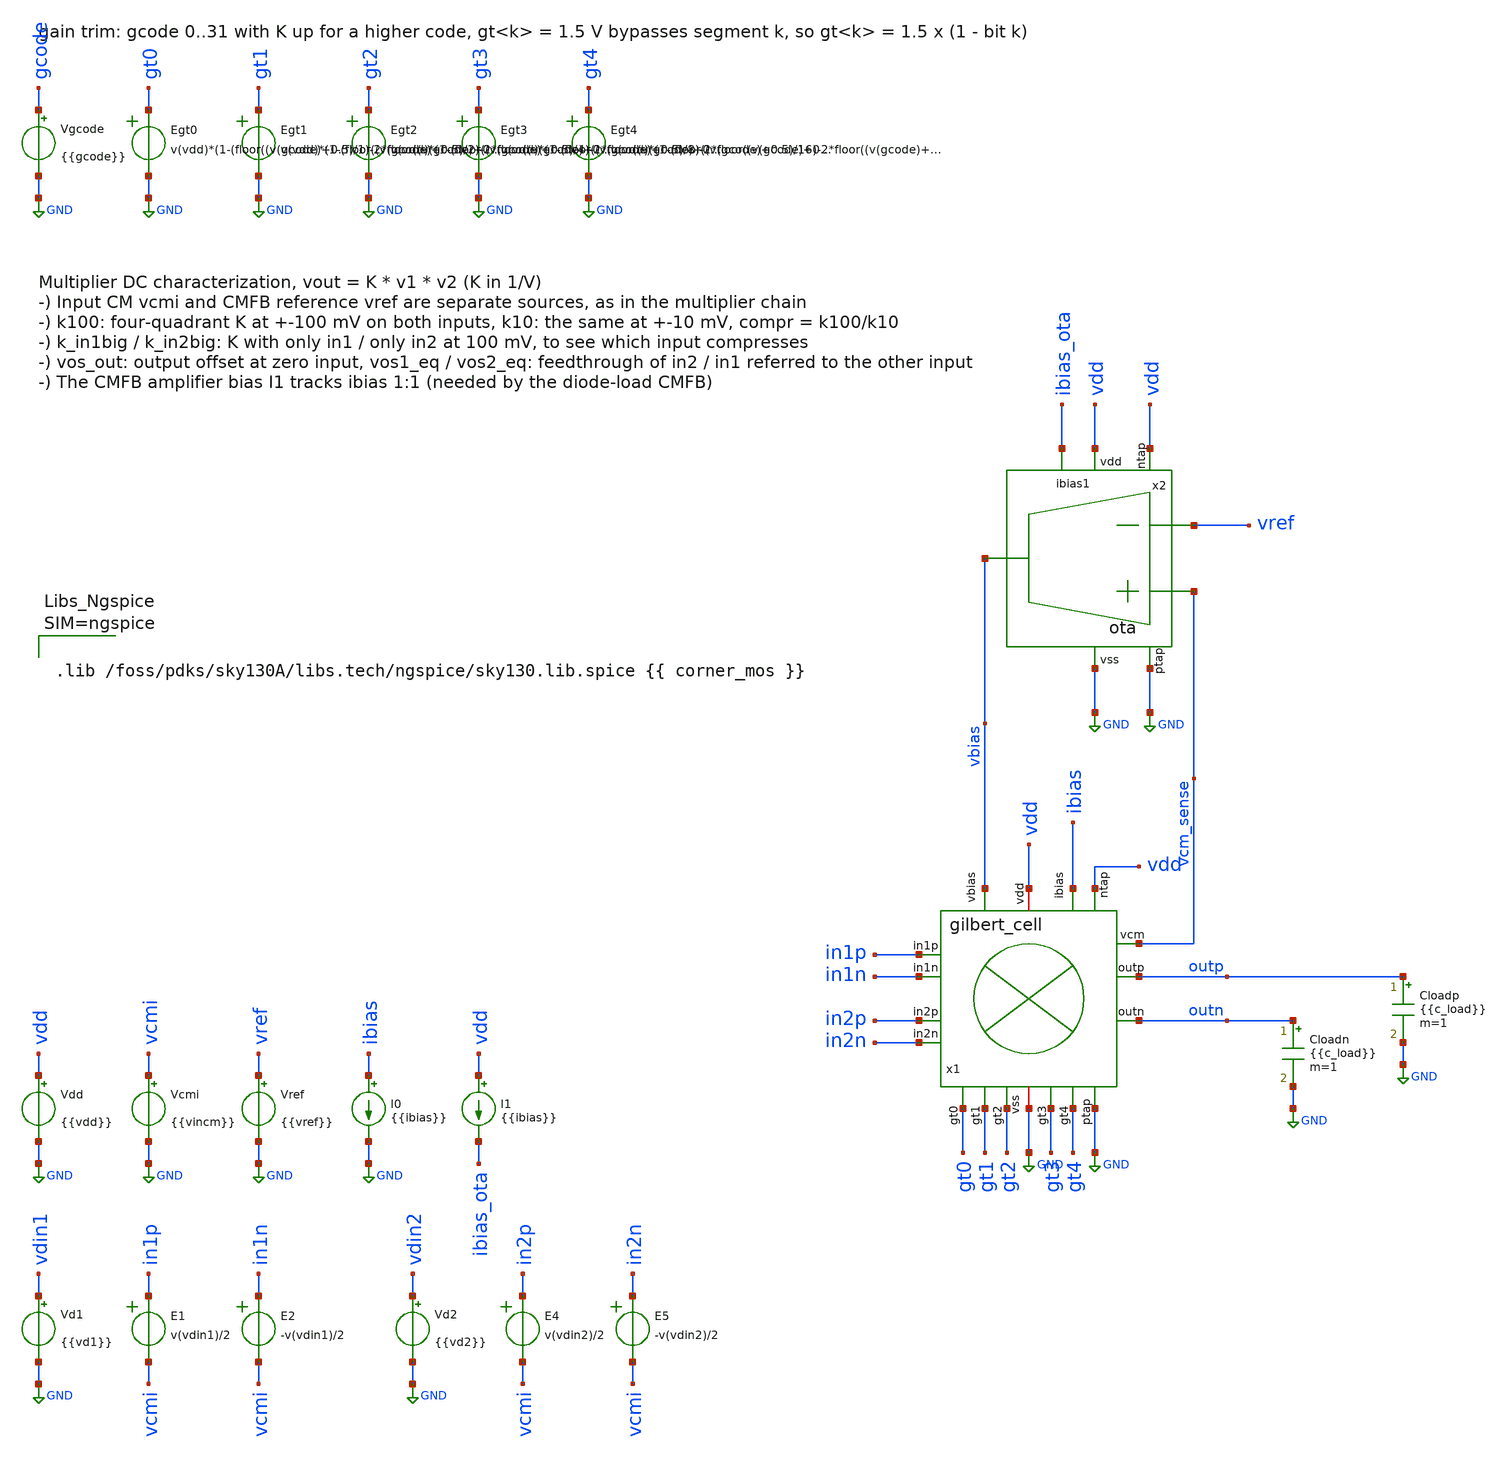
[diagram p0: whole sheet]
** sch_path: verification/porting/sky_gilbert/tb/tb_gilbert_cell_mult.sch
**.subckt tb_gilbert_cell_mult
Vdd vdd GND {{vdd}}
.save i(vdd)
Vcmi vcmi GND {{vincm}}
Vref vref GND {{vref}}
I0 ibias GND {{ibias}}
I1 vdd ibias_ota {{ibias}}
Vd1 vdin1 GND {{vd1}}
E1 in1p vcmi VOL=' v(vdin1)/2 '
E2 in1n vcmi VOL=' -v(vdin1)/2 '
Vd2 vdin2 GND {{vd2}}
E4 in2p vcmi VOL=' v(vdin2)/2 '
E5 in2n vcmi VOL=' -v(vdin2)/2 '
x1 vdd vbias outp outn in1n in1p in2p in2n GND ibias vdd GND vcm_sense gt0 gt1 gt2 gt3 gt4
+ gilbert_cell
Cloadp outp GND {{c_load}} m=1
Cloadn outn GND {{c_load}} m=1
x2 vdd vbias vref vcm_sense GND ibias_ota vdd GND ota
Vgcode gcode GND {{gcode}}
Egt0 gt0 GND VOL=' v(vdd)*(1-(floor((v(gcode)+0.5)/1)-2*floor((v(gcode)+0.5)/2))) '
Egt1 gt1 GND VOL=' v(vdd)*(1-(floor((v(gcode)+0.5)/2)-2*floor((v(gcode)+0.5)/4))) '
Egt2 gt2 GND VOL=' v(vdd)*(1-(floor((v(gcode)+0.5)/4)-2*floor((v(gcode)+0.5)/8))) '
Egt3 gt3 GND VOL=' v(vdd)*(1-(floor((v(gcode)+0.5)/8)-2*floor((v(gcode)+0.5)/16))) '
Egt4 gt4 GND VOL=' v(vdd)*(1-(floor((v(gcode)+0.5)/16)-2*floor((v(gcode)+0.5)/32))) '
**** begin user architecture code


.temp {{ temp }}
.option SEED = {{ (seed|int) + 1 }}
.option method=gear

.control
save all
* op1..op21: (vd1, vd2) points; every op plot gets vout = v(outp)-v(outn)
op
let vout = v(outp)-v(outn)
let vocm = (v(outp)+v(outn))/2
alter vd1 dc=0.1
alter vd2 dc=0.1
op
let vout = v(outp)-v(outn)
alter vd1 dc=-0.1
op
let vout = v(outp)-v(outn)
alter vd2 dc=-0.1
op
let vout = v(outp)-v(outn)
alter vd1 dc=0.1
op
let vout = v(outp)-v(outn)
* feedthrough points: one input at +-100 mV, the other at 0
alter vd2 dc=0
op
let vout = v(outp)-v(outn)
alter vd1 dc=-0.1
op
let vout = v(outp)-v(outn)
alter vd1 dc=0
alter vd2 dc=0.1
op
let vout = v(outp)-v(outn)
alter vd2 dc=-0.1
op
let vout = v(outp)-v(outn)
* small-signal four-quadrant at +-10 mV (op10..op13)
alter vd1 dc=0.01
alter vd2 dc=0.01
op
let vout = v(outp)-v(outn)
alter vd1 dc=-0.01
op
let vout = v(outp)-v(outn)
alter vd2 dc=-0.01
op
let vout = v(outp)-v(outn)
alter vd1 dc=0.01
op
let vout = v(outp)-v(outn)
* in1 at +-100 mV, in2 at +-10 mV (op14..op17)
alter vd1 dc=0.1
alter vd2 dc=0.01
op
let vout = v(outp)-v(outn)
alter vd1 dc=-0.1
op
let vout = v(outp)-v(outn)
alter vd2 dc=-0.01
op
let vout = v(outp)-v(outn)
alter vd1 dc=0.1
op
let vout = v(outp)-v(outn)
* in1 at +-10 mV, in2 at +-100 mV (op18..op21)
alter vd1 dc=0.01
alter vd2 dc=0.1
op
let vout = v(outp)-v(outn)
alter vd1 dc=-0.01
op
let vout = v(outp)-v(outn)
alter vd2 dc=-0.1
op
let vout = v(outp)-v(outn)
alter vd1 dc=0.01
op
let vout = v(outp)-v(outn)
* transfer curves: vs vd1 at vd2 = +100 mV (dc1), vs vd2 at vd1 = +100 mV (dc2)
alter vd2 dc=0.1
dc vd1 -0.2 0.2 0.005
let vout_v1 = v(outp)-v(outn)
alter vd1 dc=0.1
dc vd2 -0.2 0.2 0.005
let vout_v2 = v(outp)-v(outn)
* scalars, K = vout/(v1*v2) from four-quadrant differences (offsets and feedthrough cancel)
let k100 = (op2.vout - op3.vout - op5.vout + op4.vout)/(4*0.1*0.1)
let k10 = (op10.vout - op11.vout - op13.vout + op12.vout)/(4*0.01*0.01)
let k_in1big = (op14.vout - op15.vout - op17.vout + op16.vout)/(4*0.1*0.01)
let k_in2big = (op18.vout - op19.vout - op21.vout + op20.vout)/(4*0.01*0.1)
let compr = k100/k10
let compr1 = k_in1big/k10
let compr2 = k_in2big/k10
let vout_pp = op2.vout
let vos_out = op1.vout
let vocm = op1.vocm
* feedthrough of one input, referred to the other input as an equivalent offset
let vos2_eq = (op6.vout - op7.vout)/(2*k10*0.1)
let vos1_eq = (op8.vout - op9.vout)/(2*k10*0.1)
quit
.endc





.lib /foss/pdks/sky130A/libs.tech/ngspice/sky130.lib.spice {{ corner_mos }}



**** end user architecture code
**.ends
.GLOBAL GND
.end
